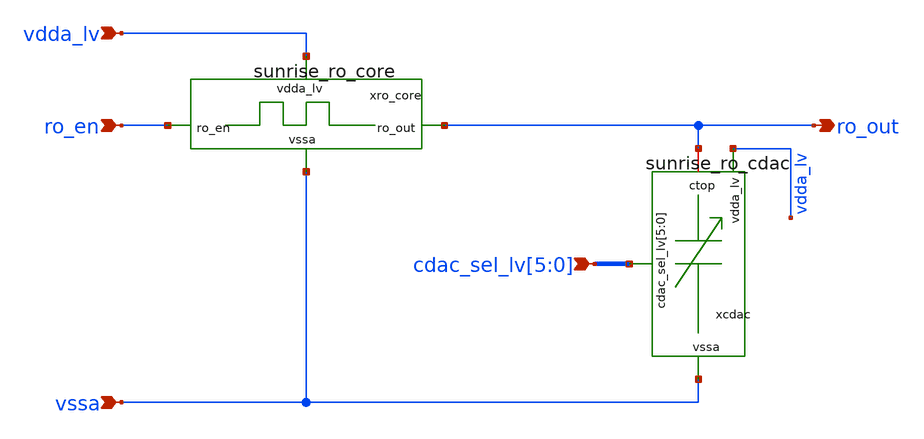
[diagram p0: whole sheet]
** sch_path: Schematics_Layout/sunrise_ro_core_wcdac/sunrise_ro_core_wcdac.sch
**.subckt sunrise_ro_core_wcdac
*+ cdac_sel_lv[5],cdac_sel_lv[4],cdac_sel_lv[3],cdac_sel_lv[2],cdac_sel_lv[1],cdac_sel_lv[0] vdda_lv vssa ro_en ro_out
*.ipin cdac_sel_lv[5],cdac_sel_lv[4],cdac_sel_lv[3],cdac_sel_lv[2],cdac_sel_lv[1],cdac_sel_lv[0]
*.ipin vdda_lv
*.ipin vssa
*.ipin ro_en
*.opin ro_out
xro_core vdda_lv vssa ro_en ro_out sunrise_ro_core
xcdac cdac_sel_lv[5] cdac_sel_lv[4] cdac_sel_lv[3] cdac_sel_lv[2] cdac_sel_lv[1] cdac_sel_lv[0]
+ ro_out vssa vdda_lv sunrise_ro_cdac
**.ends
.end
